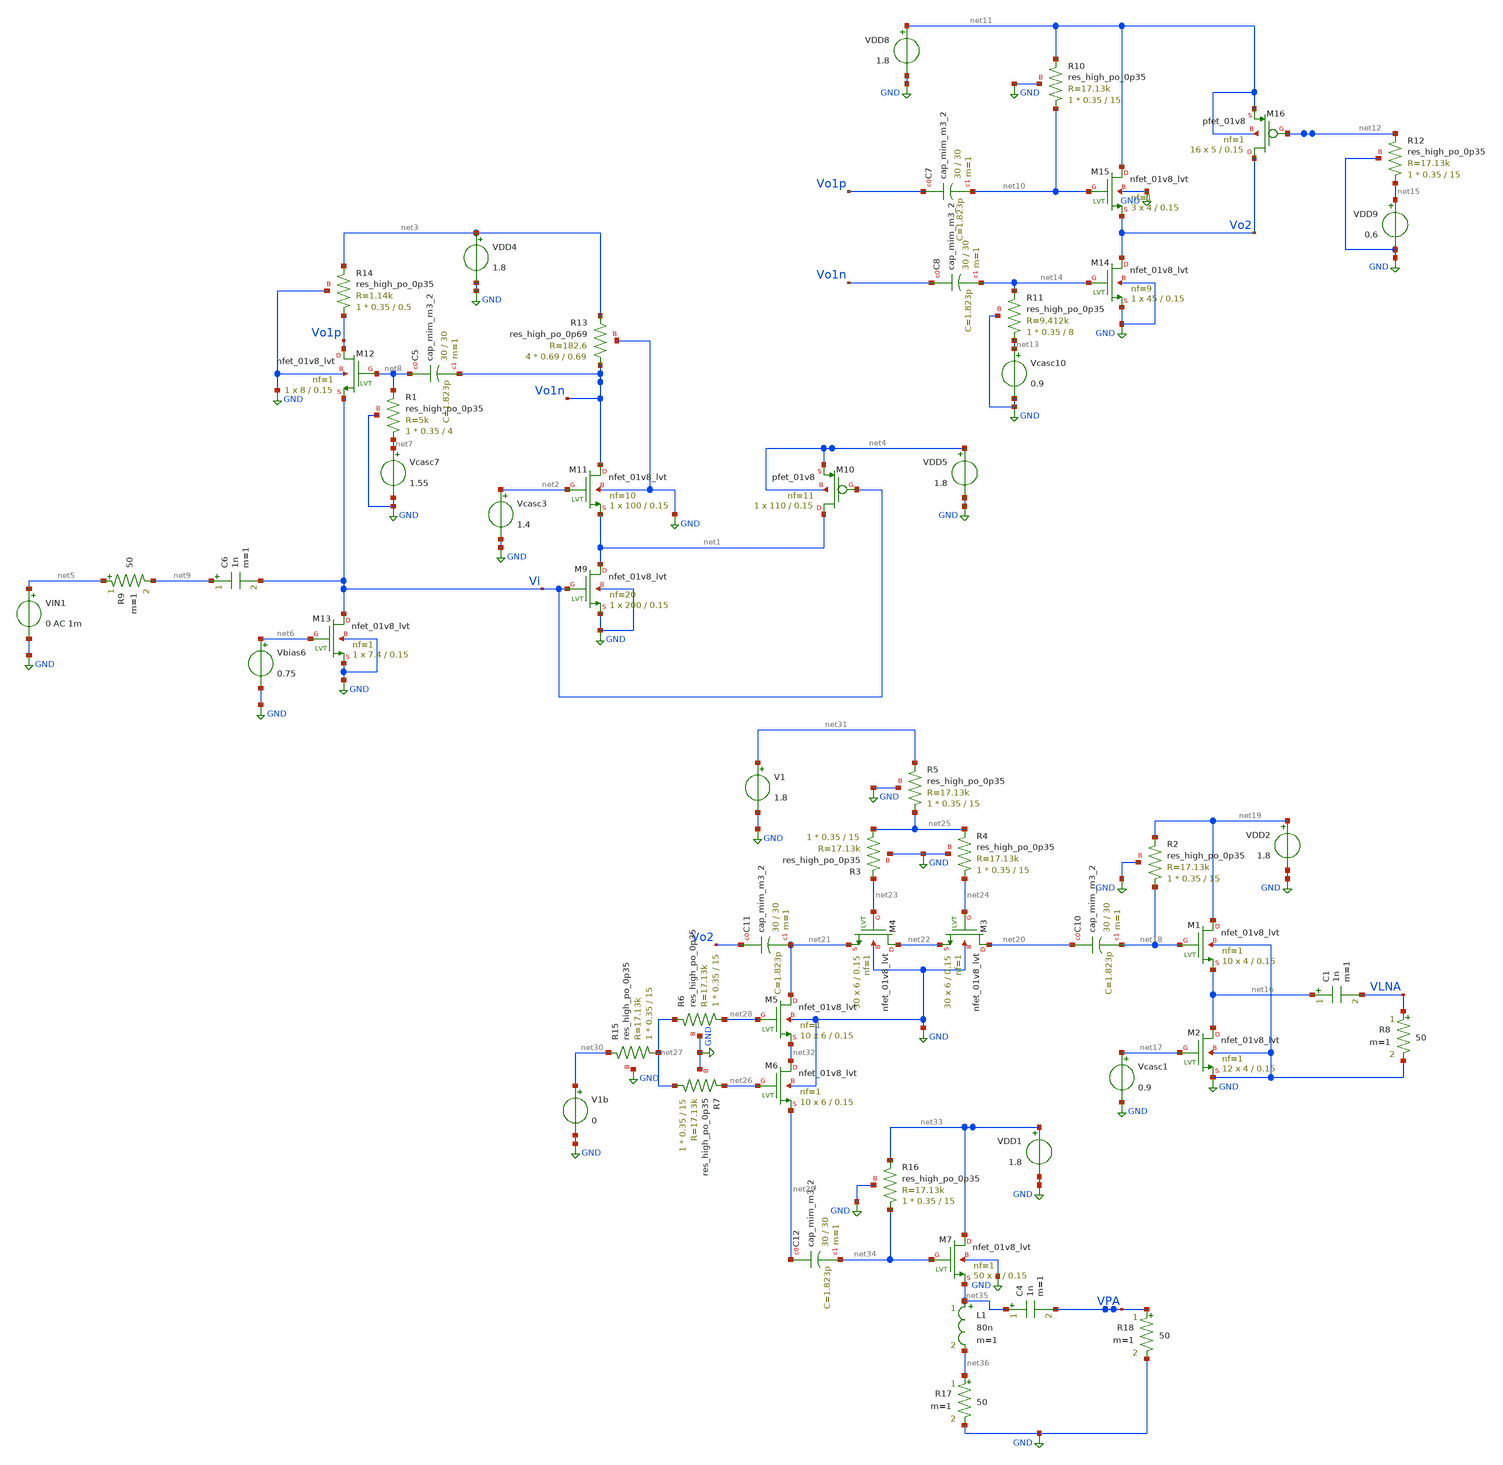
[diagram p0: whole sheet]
** sch_path: xschem/CompleteAMP.sch
**.subckt CompleteAMP
VIN1 net5 GND 0 AC 1m
Vcasc3 net2 GND 1.4
VDD4 net3 GND 1.8
VDD5 net4 GND 1.8
Vbias6 net6 GND 0.75
Vcasc7 net7 GND 1.55
XR1 net7 net8 GND sky130_fd_pr__res_high_po_0p35 L=4 mult=1 m=1
XC5 net8 Vo1n sky130_fd_pr__cap_mim_m3_2 W=30 L=30 MF=1 m=1
C6 net9 Vi 1n m=1
XM9 net1 Vi GND GND sky130_fd_pr__nfet_01v8_lvt L=0.15 W=200 nf=20 ad='int((nf+1)/2) * W/nf * 0.29' as='int((nf+2)/2) * W/nf * 0.29'
+ pd='2*int((nf+1)/2) * (W/nf + 0.29)' ps='2*int((nf+2)/2) * (W/nf + 0.29)' nrd='0.29 / W' nrs='0.29 / W'
+ sa=0 sb=0 sd=0 mult=1 m=1
XM10 net1 Vi net4 net4 sky130_fd_pr__pfet_01v8 L=0.15 W=110 nf=11 ad='int((nf+1)/2) * W/nf * 0.29' as='int((nf+2)/2) * W/nf * 0.29'
+ pd='2*int((nf+1)/2) * (W/nf + 0.29)' ps='2*int((nf+2)/2) * (W/nf + 0.29)' nrd='0.29 / W' nrs='0.29 / W'
+ sa=0 sb=0 sd=0 mult=1 m=1
XM11 Vo1n net2 net1 GND sky130_fd_pr__nfet_01v8_lvt L=0.15 W=100 nf=10 ad='int((nf+1)/2) * W/nf * 0.29'
+ as='int((nf+2)/2) * W/nf * 0.29' pd='2*int((nf+1)/2) * (W/nf + 0.29)' ps='2*int((nf+2)/2) * (W/nf + 0.29)'
+ nrd='0.29 / W' nrs='0.29 / W' sa=0 sb=0 sd=0 mult=1 m=1
XM12 Vo1p net8 Vi GND sky130_fd_pr__nfet_01v8_lvt L=0.15 W=8 nf=1 ad='int((nf+1)/2) * W/nf * 0.29' as='int((nf+2)/2) * W/nf * 0.29'
+ pd='2*int((nf+1)/2) * (W/nf + 0.29)' ps='2*int((nf+2)/2) * (W/nf + 0.29)' nrd='0.29 / W' nrs='0.29 / W'
+ sa=0 sb=0 sd=0 mult=1 m=1
XM13 Vi net6 GND GND sky130_fd_pr__nfet_01v8_lvt L=0.15 W=7.4 nf=1 ad='int((nf+1)/2) * W/nf * 0.29' as='int((nf+2)/2) * W/nf * 0.29'
+ pd='2*int((nf+1)/2) * (W/nf + 0.29)' ps='2*int((nf+2)/2) * (W/nf + 0.29)' nrd='0.29 / W' nrs='0.29 / W'
+ sa=0 sb=0 sd=0 mult=1 m=1
R9 net5 net9 50 m=1
XM14 Vo2 net14 GND GND sky130_fd_pr__nfet_01v8_lvt L=0.15 W=45 nf=9 ad='int((nf+1)/2) * W/nf * 0.29'
+ as='int((nf+2)/2) * W/nf * 0.29' pd='2*int((nf+1)/2) * (W/nf + 0.29)' ps='2*int((nf+2)/2) * (W/nf + 0.29)'
+ nrd='0.29 / W' nrs='0.29 / W' sa=0 sb=0 sd=0 mult=1 m=1
XM15 net11 net10 Vo2 GND sky130_fd_pr__nfet_01v8_lvt L=0.15 W=4 nf=1 ad='int((nf+1)/2) * W/nf * 0.29'
+ as='int((nf+2)/2) * W/nf * 0.29' pd='2*int((nf+1)/2) * (W/nf + 0.29)' ps='2*int((nf+2)/2) * (W/nf + 0.29)'
+ nrd='0.29 / W' nrs='0.29 / W' sa=0 sb=0 sd=0 mult=3 m=3
XR10 net10 net11 GND sky130_fd_pr__res_high_po_0p35 L=15 mult=1 m=1
XM16 Vo2 net12 net11 net11 sky130_fd_pr__pfet_01v8 L=0.15 W=5 nf=1 ad='int((nf+1)/2) * W/nf * 0.29' as='int((nf+2)/2) * W/nf * 0.29'
+ pd='2*int((nf+1)/2) * (W/nf + 0.29)' ps='2*int((nf+2)/2) * (W/nf + 0.29)' nrd='0.29 / W' nrs='0.29 / W'
+ sa=0 sb=0 sd=0 mult=16 m=16
VDD8 net11 GND 1.8
VDD9 net15 GND 0.6
XC7 Vo1p net10 sky130_fd_pr__cap_mim_m3_2 W=30 L=30 MF=1 m=1
Vcasc10 net13 GND 0.9
XR11 net13 net14 GND sky130_fd_pr__res_high_po_0p35 L=8 mult=1 m=1
XC8 Vo1n net14 sky130_fd_pr__cap_mim_m3_2 W=30 L=30 MF=1 m=1
XR12 net15 net12 GND sky130_fd_pr__res_high_po_0p35 L=15 mult=1 m=1
XR13 Vo1n net3 GND sky130_fd_pr__res_high_po_0p69 L=0.69 mult=4 m=4
XR14 Vo1p net3 GND sky130_fd_pr__res_high_po_0p35 L=0.5 mult=1 m=1
XM1 net19 net18 net16 GND sky130_fd_pr__nfet_01v8_lvt L=0.15 W=4 nf=1 ad='int((nf+1)/2) * W/nf * 0.29'
+ as='int((nf+2)/2) * W/nf * 0.29' pd='2*int((nf+1)/2) * (W/nf + 0.29)' ps='2*int((nf+2)/2) * (W/nf + 0.29)'
+ nrd='0.29 / W' nrs='0.29 / W' sa=0 sb=0 sd=0 mult=10 m=10
XM2 net16 net17 GND GND sky130_fd_pr__nfet_01v8_lvt L=0.15 W=4 nf=1 ad='int((nf+1)/2) * W/nf * 0.29'
+ as='int((nf+2)/2) * W/nf * 0.29' pd='2*int((nf+1)/2) * (W/nf + 0.29)' ps='2*int((nf+2)/2) * (W/nf + 0.29)'
+ nrd='0.29 / W' nrs='0.29 / W' sa=0 sb=0 sd=0 mult=12 m=12
C1 net16 VLNA 1n m=1
R8 VLNA GND 50 m=1
Vcasc1 net17 GND 0.9
XC10 net20 net18 sky130_fd_pr__cap_mim_m3_2 W=30 L=30 MF=1 m=1
XR2 net18 net19 GND sky130_fd_pr__res_high_po_0p35 L=15 mult=1 m=1
VDD2 net19 GND 1.8
XM3 net20 net24 net22 GND sky130_fd_pr__nfet_01v8_lvt L=0.15 W=6 nf=1 ad='int((nf+1)/2) * W/nf * 0.29'
+ as='int((nf+2)/2) * W/nf * 0.29' pd='2*int((nf+1)/2) * (W/nf + 0.29)' ps='2*int((nf+2)/2) * (W/nf + 0.29)'
+ nrd='0.29 / W' nrs='0.29 / W' sa=0 sb=0 sd=0 mult=30 m=30
XM4 net22 net23 net21 GND sky130_fd_pr__nfet_01v8_lvt L=0.15 W=6 nf=1 ad='int((nf+1)/2) * W/nf * 0.29'
+ as='int((nf+2)/2) * W/nf * 0.29' pd='2*int((nf+1)/2) * (W/nf + 0.29)' ps='2*int((nf+2)/2) * (W/nf + 0.29)'
+ nrd='0.29 / W' nrs='0.29 / W' sa=0 sb=0 sd=0 mult=30 m=30
XM5 net21 net28 net32 GND sky130_fd_pr__nfet_01v8_lvt L=0.15 W=6 nf=1 ad='int((nf+1)/2) * W/nf * 0.29'
+ as='int((nf+2)/2) * W/nf * 0.29' pd='2*int((nf+1)/2) * (W/nf + 0.29)' ps='2*int((nf+2)/2) * (W/nf + 0.29)'
+ nrd='0.29 / W' nrs='0.29 / W' sa=0 sb=0 sd=0 mult=10 m=10
XM6 net32 net26 net29 GND sky130_fd_pr__nfet_01v8_lvt L=0.15 W=6 nf=1 ad='int((nf+1)/2) * W/nf * 0.29'
+ as='int((nf+2)/2) * W/nf * 0.29' pd='2*int((nf+1)/2) * (W/nf + 0.29)' ps='2*int((nf+2)/2) * (W/nf + 0.29)'
+ nrd='0.29 / W' nrs='0.29 / W' sa=0 sb=0 sd=0 mult=10 m=10
XR3 net25 net23 GND sky130_fd_pr__res_high_po_0p35 L=15 mult=1 m=1
XR4 net24 net25 GND sky130_fd_pr__res_high_po_0p35 L=15 mult=1 m=1
XR5 net25 net31 GND sky130_fd_pr__res_high_po_0p35 L=15 mult=1 m=1
V1b net30 GND 0
XR6 net28 net27 GND sky130_fd_pr__res_high_po_0p35 L=15 mult=1 m=1
XR7 net27 net26 GND sky130_fd_pr__res_high_po_0p35 L=15 mult=1 m=1
XR15 net27 net30 GND sky130_fd_pr__res_high_po_0p35 L=15 mult=1 m=1
V1 net31 GND 1.8
XC11 Vo2 net21 sky130_fd_pr__cap_mim_m3_2 W=30 L=30 MF=1 m=1
XM7 net33 net34 net35 GND sky130_fd_pr__nfet_01v8_lvt L=0.15 W=4 nf=1 ad='int((nf+1)/2) * W/nf * 0.29'
+ as='int((nf+2)/2) * W/nf * 0.29' pd='2*int((nf+1)/2) * (W/nf + 0.29)' ps='2*int((nf+2)/2) * (W/nf + 0.29)'
+ nrd='0.29 / W' nrs='0.29 / W' sa=0 sb=0 sd=0 mult=50 m=50
VDD1 net33 GND 1.8
XR16 net34 net33 GND sky130_fd_pr__res_high_po_0p35 L=15 mult=1 m=1
L1 net35 net36 80n m=1
C4 net35 VPA 1n m=1
R17 net36 GND 50 m=1
R18 VPA GND 50 m=1
XC12 net29 net34 sky130_fd_pr__cap_mim_m3_2 W=30 L=30 MF=1 m=1
**** begin user architecture code

.lib $::SKYWATER_MODELS/sky130.lib.spice tt




.control
save all
op
	let gm1=@m.xm1.msky130_fd_pr__nfet_01v8_lvt[gm]
	let id1=@m.xm1.msky130_fd_pr__nfet_01v8_lvt[id]
	let gm2=@m.xm2.msky130_fd_pr__pfet_01v8[gm]
	let id2=@m.xm2.msky130_fd_pr__pfet_01v8[id]
	let gm3=@m.xm3.msky130_fd_pr__nfet_01v8_lvt[gm]
	let id3=@m.xm3.msky130_fd_pr__nfet_01v8_lvt[id]
	let gm4=@m.xm4.msky130_fd_pr__nfet_01v8_lvt[gm]
	let id4=@m.xm4.msky130_fd_pr__nfet_01v8_lvt[id]
	let gm5=@m.xm5.msky130_fd_pr__nfet_01v8_lvt[gm]
	let id5=@m.xm5.msky130_fd_pr__nfet_01v8_lvt[id]
	let gm6=@m.xm6.msky130_fd_pr__nfet_01v8_lvt[gm]
	let id6=@m.xm6.msky130_fd_pr__nfet_01v8_lvt[id]
	let gm7=@m.xm7.msky130_fd_pr__nfet_01v8_lvt[gm]
	let id7=@m.xm7.msky130_fd_pr__nfet_01v8_lvt[id]
	let gm8=@m.xm8.msky130_fd_pr__nfet_01v8_lvt[gm]
	let id8=@m.xm8.msky130_fd_pr__nfet_01v8_lvt[id]
	print id1 gm1
	print id2 gm2
	print id3 gm3
	print id4 gm4
	print id5 gm5
	print id6 gm6
	print id7 gm7
	print id8 gm8
	print v(vi)
	print v(vo1n)
	print v(vo1p)

ac dec 40 0.1G 10G

let Zo=50;
let Zin=v(vi)/-i(VIN1)
Let S11=mag( (Zin-Zo)/(Zin+Zo) )
plot db(S11)
WRDATA S11.csv db(S11)
plot mag(Zin);



let G1p=db(v(Vo1p)/v(Vi))
let G1n=db(v(Vo1n)/v(Vi))
let G2=db(v(Vo2)/v(Vi))

let GLNA=db(v(VLNA)/v(Vi))
let GPA=db(v(VPA)/v(Vi))

plot G1p G1n G2 GLNA GPA
WRDATA Gain.csv GLNA GPA
set sqrnoise

noise v(Vo1n) VIN1 dec 40 1G 10G
setplot noise1
let Fn=inoise_spectrum/(8.3e-19)
let NFn=db(Fn) / 2
plot NFn

noise v(Vo1p) VIN1 dec 40 1G 10G
setplot noise1
let Fp=inoise_spectrum/(8.3e-19)
let NFp=db(Fp) / 2
plot NFp

noise v(Vo1p) VIN1 dec 40 1G 10G
setplot noise1
let F2=inoise_spectrum/(8.3e-19)
let NF2=db(F2) / 2
plot NF2

noise v(VLNA) VIN1 dec 40 1G 10G
setplot noise1
let Fo=inoise_spectrum/(8.3e-19)
let NFo=db(Fo) / 2
plot NFo

WRData Noise.csv NF2

.endc


**** end user architecture code
**.ends
.GLOBAL GND
.end
